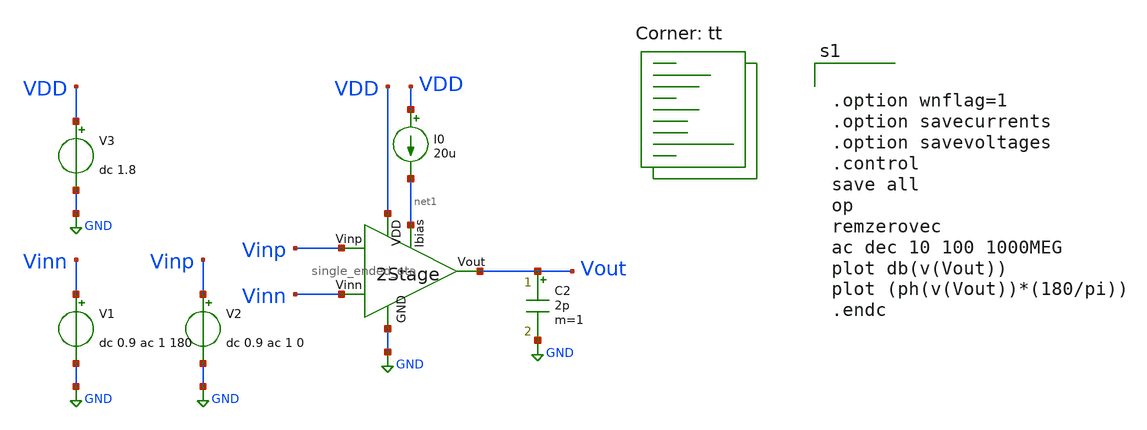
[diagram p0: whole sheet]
** sch_path: schematic/single_ended_test.sch
**.subckt single_ended_test
V1 Vinn GND dc 0.9 ac 1 180
V2 Vinp GND dc 0.9 ac 1 0
V3 VDD GND dc 1.8
I0 VDD net1 20u
C2 Vout GND 2p m=1
x1 VDD GND net1 Vout Vinp Vinn single_ended_ota
**** begin user architecture code
.lib $::SKYWATER_MODELS/sky130.lib.spice tt


.option wnflag=1
.option savecurrents
.option savevoltages
.control
save all
op
remzerovec
ac dec 10 100 1000MEG
plot db(v(Vout))
plot (ph(v(Vout))*(180/pi))
.endc


**** end user architecture code
**.ends

* expanding   symbol:  single_ended_ota.sym # of pins=6
** sym_path: schematic/single_ended_ota.sym
** sch_path: schematic/single_ended_ota.sch
.subckt single_ended_ota VDD GND Ibias Vout Vinp Vinn
*.opin Vout
*.ipin Vinn
*.ipin Vinp
*.ipin Ibias
*.ipin VDD
*.ipin GND
XM1 net1 Vinn net2 GND sky130_fd_pr__nfet_01v8_lvt L=0.75 W=11 nf=1 ad='int((nf+1)/2) * W/nf * 0.29'
+ as='int((nf+2)/2) * W/nf * 0.29' pd='2*int((nf+1)/2) * (W/nf + 0.29)' ps='2*int((nf+2)/2) * (W/nf + 0.29)'
+ nrd='0.29 / W' nrs='0.29 / W' sa=0 sb=0 sd=0 mult=1 m=1
XM2 net1 net1 VDD VDD sky130_fd_pr__pfet_01v8_lvt L=0.75 W=11 nf=1 ad='int((nf+1)/2) * W/nf * 0.29' as='int((nf+2)/2) * W/nf * 0.29'
+ pd='2*int((nf+1)/2) * (W/nf + 0.29)' ps='2*int((nf+2)/2) * (W/nf + 0.29)' nrd='0.29 / W' nrs='0.29 / W'
+ sa=0 sb=0 sd=0 mult=3 m=3
XM3 V1 Vinp net2 GND sky130_fd_pr__nfet_01v8_lvt L=0.75 W=11 nf=1 ad='int((nf+1)/2) * W/nf * 0.29' as='int((nf+2)/2) * W/nf * 0.29'
+ pd='2*int((nf+1)/2) * (W/nf + 0.29)' ps='2*int((nf+2)/2) * (W/nf + 0.29)' nrd='0.29 / W' nrs='0.29 / W'
+ sa=0 sb=0 sd=0 mult=1 m=1
XM4 V1 net1 VDD VDD sky130_fd_pr__pfet_01v8_lvt L=0.75 W=11 nf=1 ad='int((nf+1)/2) * W/nf * 0.29' as='int((nf+2)/2) * W/nf * 0.29'
+ pd='2*int((nf+1)/2) * (W/nf + 0.29)' ps='2*int((nf+2)/2) * (W/nf + 0.29)' nrd='0.29 / W' nrs='0.29 / W'
+ sa=0 sb=0 sd=0 mult=3 m=3
XM5 net2 Ibias GND GND sky130_fd_pr__nfet_01v8_lvt L=1 W=20 nf=1 ad='int((nf+1)/2) * W/nf * 0.29' as='int((nf+2)/2) * W/nf * 0.29'
+ pd='2*int((nf+1)/2) * (W/nf + 0.29)' ps='2*int((nf+2)/2) * (W/nf + 0.29)' nrd='0.29 / W' nrs='0.29 / W'
+ sa=0 sb=0 sd=0 mult=1 m=1
XM6 Vout Ibias GND GND sky130_fd_pr__nfet_01v8_lvt L=1 W=80 nf=1 ad='int((nf+1)/2) * W/nf * 0.29' as='int((nf+2)/2) * W/nf * 0.29'
+ pd='2*int((nf+1)/2) * (W/nf + 0.29)' ps='2*int((nf+2)/2) * (W/nf + 0.29)' nrd='0.29 / W' nrs='0.29 / W'
+ sa=0 sb=0 sd=0 mult=1 m=1
XM7 Vout V1 VDD VDD sky130_fd_pr__pfet_01v8_lvt L=0.6 W=200 nf=1 ad='int((nf+1)/2) * W/nf * 0.29' as='int((nf+2)/2) * W/nf * 0.29'
+ pd='2*int((nf+1)/2) * (W/nf + 0.29)' ps='2*int((nf+2)/2) * (W/nf + 0.29)' nrd='0.29 / W' nrs='0.29 / W'
+ sa=0 sb=0 sd=0 mult=1 m=1
R1 net3 V1 1000 m=1
C1 Vout net3 1.4p m=1
XM10 Ibias Ibias GND GND sky130_fd_pr__nfet_01v8_lvt L=1 W=4 nf=1 ad='int((nf+1)/2) * W/nf * 0.29' as='int((nf+2)/2) * W/nf * 0.29'
+ pd='2*int((nf+1)/2) * (W/nf + 0.29)' ps='2*int((nf+2)/2) * (W/nf + 0.29)' nrd='0.29 / W' nrs='0.29 / W'
+ sa=0 sb=0 sd=0 mult=1 m=1
.ends

.GLOBAL GND
.end
